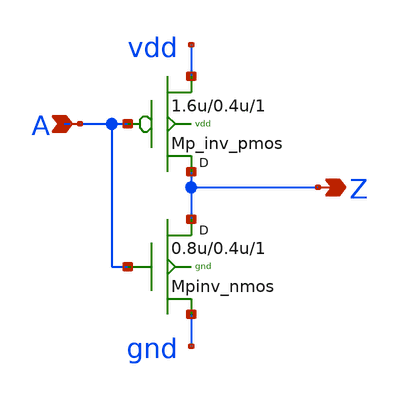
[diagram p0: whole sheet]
** sch_path: sram_2_16_scn4m/pinv_8.sch
**.subckt pinv_8 A Z
*.ipin A
*.opin Z
Mpinv_nmos Z A gnd gnd n w=0.8u l=0.4u m=1
Mp_inv_pmos Z A vdd vdd p w=1.6u l=0.4u m=1
**.ends
.end
